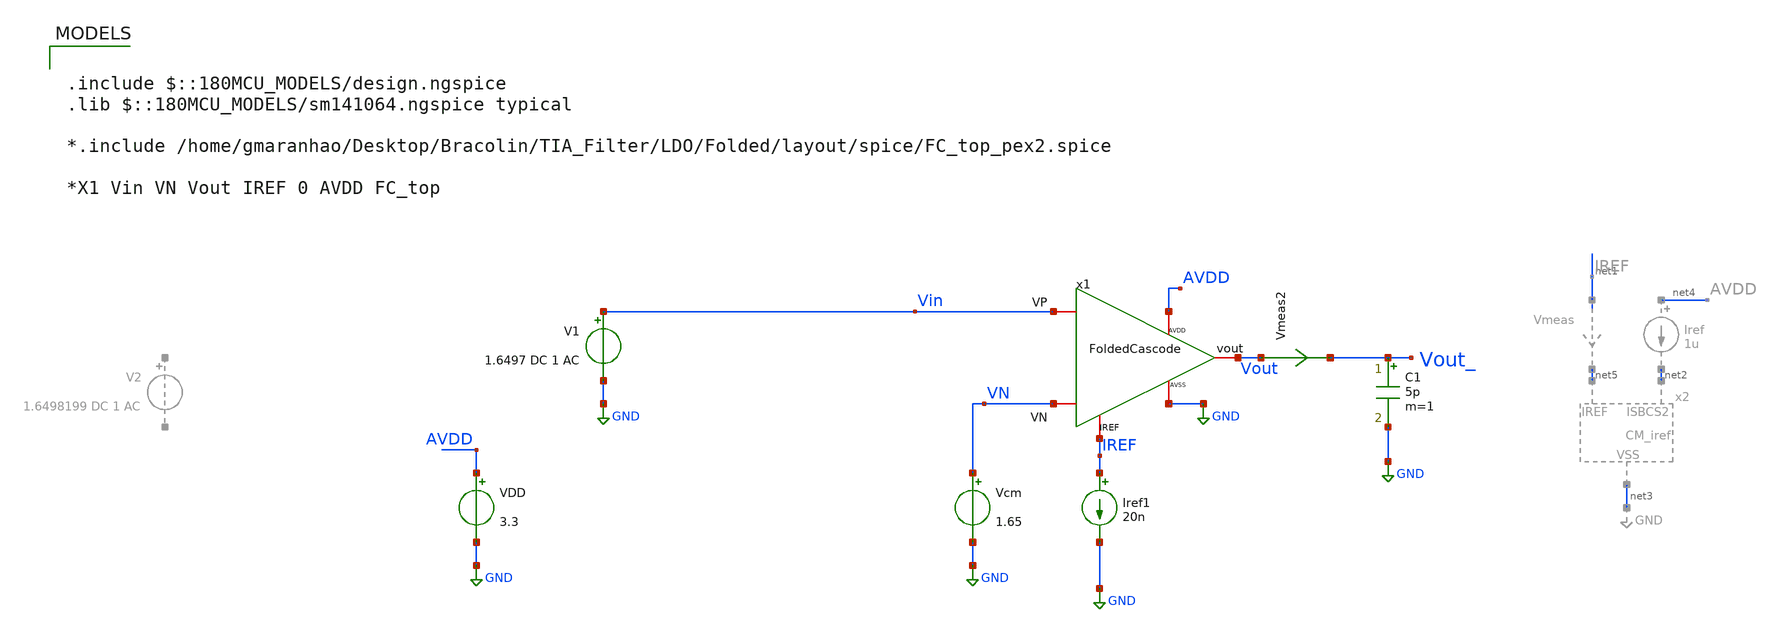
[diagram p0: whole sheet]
** sch_path: Voltage_Reference/LDO/Folded/TB_Folded_dc.sch
**.subckt TB_Folded_dc
VDD AVDD GND 3.3
Vcm VN GND 1.65
Vmeas2 Vout Vout_ 0
.save i(vmeas2)
C1 Vout_ GND 5p m=1
x1 Vin VN Vout IREF AVDD GND FoldedCascode
V1 Vin GND 1.6497 DC 1 AC
Iref1 IREF GND 20n
**** begin user architecture code

.include $::180MCU_MODELS/design.ngspice
.lib $::180MCU_MODELS/sm141064.ngspice typical

*.include /home/gmaranhao/Desktop/Bracolin/TIA_Filter/LDO/Folded/layout/spice/FC_top_pex2.spice

*X1 Vin VN Vout IREF 0 AVDD FC_top



.option gmin=1e-18



.control
save all

*set temp=80

op
remzerovec
write TB_Folded_dc.raw
set appendwrite

*dc V1 1.648 1.651 0.001m
*remzerovec
*write TB_Folded_dc.raw
*wrdata /home/gmaranhao/Desktop/Bracolin/TIA_Filter/LDO/Folded/plots/DC-AC/Folded_DC_PEX.txt V(Vout)



ac dec 10 1m 1e9
remzerovec
write TB_Folded_dc.raw
wrdata /home/gmaranhao/Desktop/Bracolin/TIA_Filter/LDO/Folded/plots/DC-AC/Folded_AC_20n.txt V(Vout)


.endc


**** end user architecture code
**.ends
.GLOBAL GND
.end
